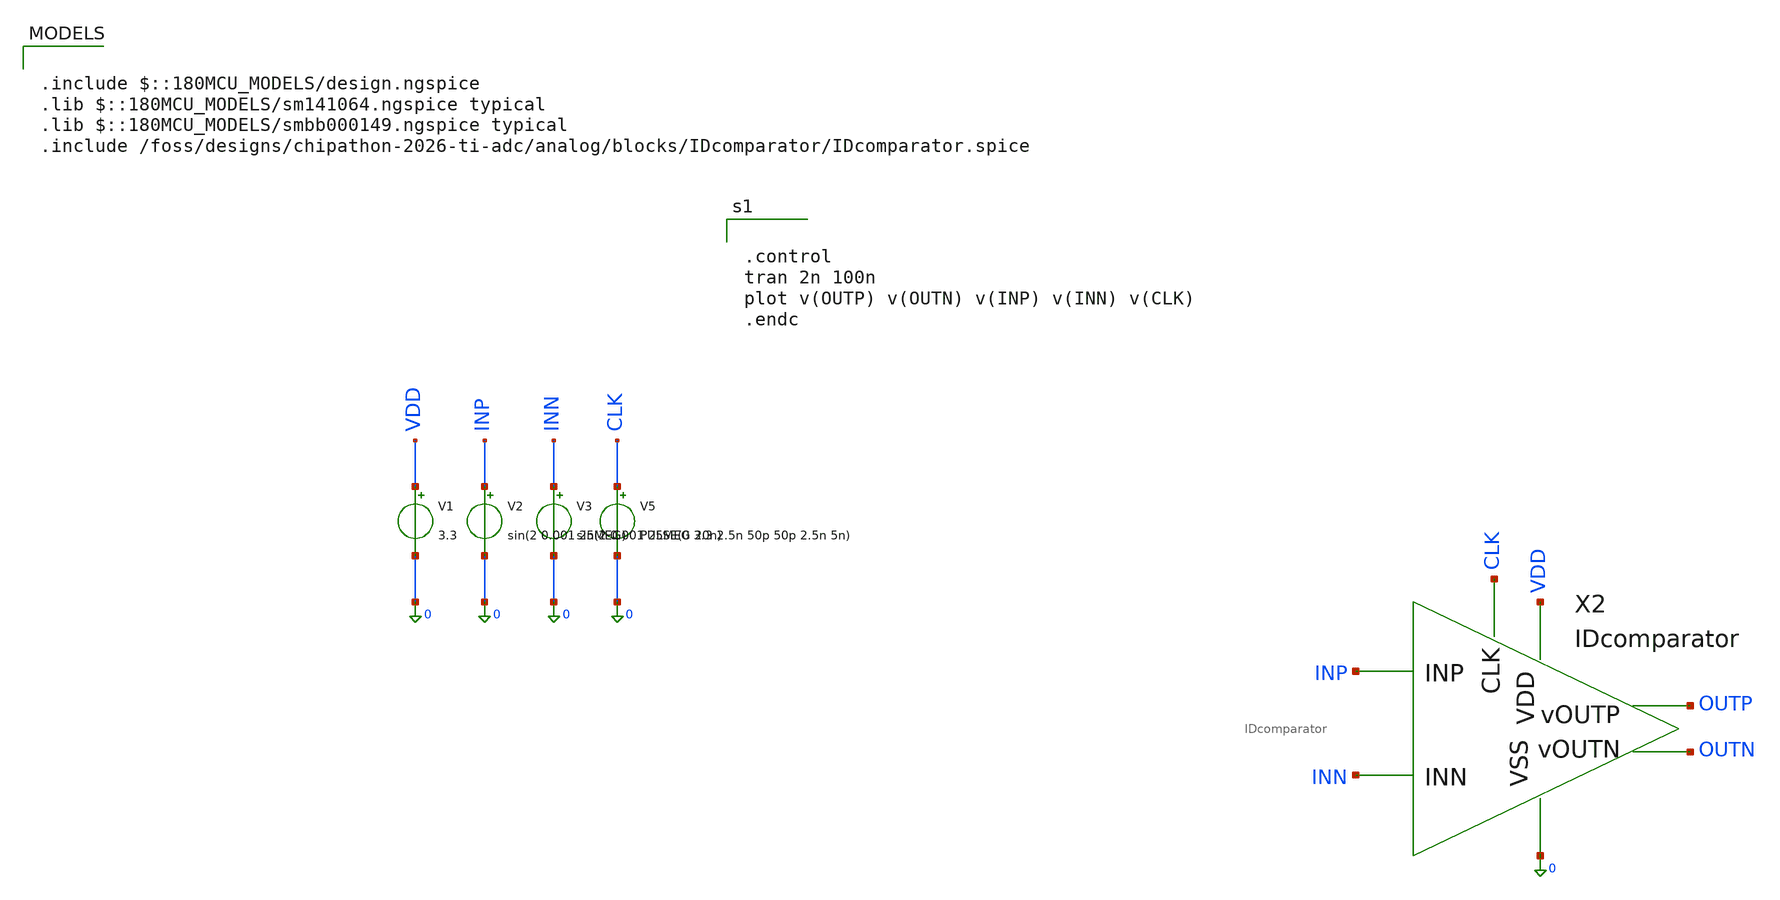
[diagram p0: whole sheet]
** sch_path: analog/blocks/Double_Tail_Comparator/realcomptest.sch
**.subckt realcomptest
V1 VDD 0 3.3
V2 INP 0 sin(2 0.001 25MEG)
V3 INN 0 sin(2 0.001 25MEG 20n)
V5 CLK 0 PULSE(0 3.3 2.5n 50p 50p 2.5n 5n)
X2 INP INN CLK VDD 0 OUTP OUTN IDcomparator
**** begin user architecture code

.include $::180MCU_MODELS/design.ngspice
.lib $::180MCU_MODELS/sm141064.ngspice typical
.lib $::180MCU_MODELS/smbb000149.ngspice typical
.include /foss/designs/chipathon-2026-ti-adc/analog/blocks/IDcomparator/IDcomparator.spice



.control
tran 2n 100n
plot v(OUTP) v(OUTN) v(INP) v(INN) v(CLK)
.endc


**** end user architecture code
**.ends
.end
